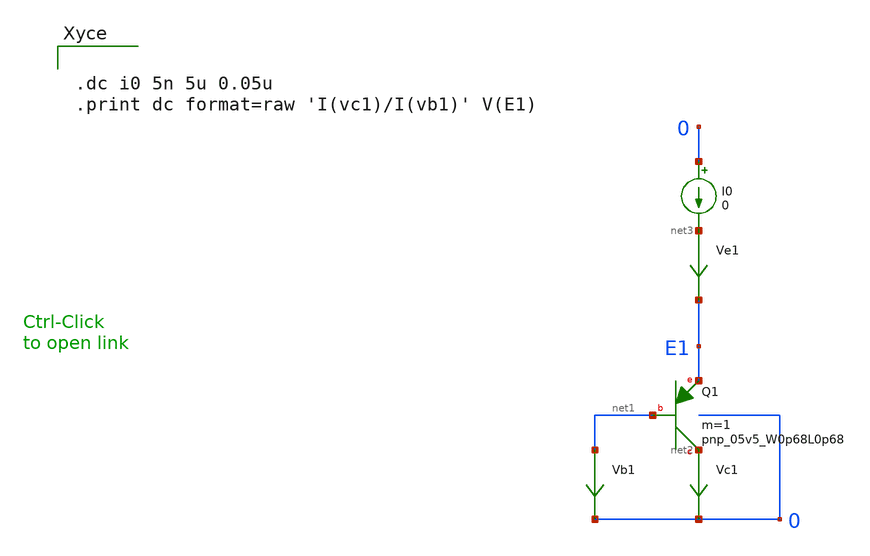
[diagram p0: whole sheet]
** sch_path: sky130_tests_X/test_bipolar2x.sch
* Copyright 2020 Stefan Frederik Schippers
* Licensed under the Apache License, Version 2.0 (the "License");
* you may not use this file except in compliance with the License.
* You may obtain a copy of the License at
* https://www.apache.org/licenses/LICENSE-2.0
* Unless required by applicable law or agreed to in writing, software
* distributed under the License is distributed on an "AS IS" BASIS,
* WITHOUT WARRANTIES OR CONDITIONS OF ANY KIND, either express or implied.
* See the License for the specific language governing permissions and
* limitations under the License.
**.subckt test_bipolar2x
XQ1 net2 net1 E1 sky130_fd_pr__pnp_05v5_W0p68L0p68 m=1
Vc1 net2 0 0
.save i(vc1)
Vb1 net1 0 0
.save i(vb1)
I0 0 net3 0
Ve1 net3 E1 0
.save i(ve1)
**** begin user architecture code


.dc i0 5n 5u 0.05u
.print dc format=raw 'I(vc1)/I(vb1)' V(E1)



**** end user architecture code
**.ends
.end
